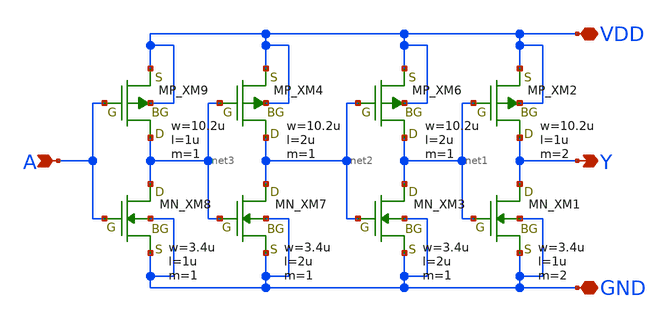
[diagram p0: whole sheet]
** sch_path: openIP62_rev1.0/IP62/Technology/tech/symbols/Xschem/IP62_5_stdcell/DEL1.sch
**.subckt DEL1 A Y VDD GND
*.ipin A
*.opin Y
*.iopin VDD
*.iopin GND
XM9 net3 A VDD VDD PMOS w=10.2u l=1u as=0 ad=0 ps=0 pd=0 nrd=0 nrs=0 m=1
XM2 Y net1 VDD VDD PMOS w=10.2u l=1u as=0 ad=0 ps=0 pd=0 nrd=0 nrs=0 m=2
XM8 net3 A GND GND NMOS w=3.4u l=1u as=0 ad=0 ps=0 pd=0 nrd=0 nrs=0 m=1
XM1 Y net1 GND GND NMOS w=3.4u l=1u as=0 ad=0 ps=0 pd=0 nrd=0 nrs=0 m=2
XM4 net2 net3 VDD VDD PMOS w=10.2u l=2u as=0 ad=0 ps=0 pd=0 nrd=0 nrs=0 m=1
XM6 net1 net2 VDD VDD PMOS w=10.2u l=2u as=0 ad=0 ps=0 pd=0 nrd=0 nrs=0 m=1
XM7 net2 net3 GND GND NMOS w=3.4u l=2u as=0 ad=0 ps=0 pd=0 nrd=0 nrs=0 m=1
XM3 net1 net2 GND GND NMOS w=3.4u l=2u as=0 ad=0 ps=0 pd=0 nrd=0 nrs=0 m=1
**.ends
.end
